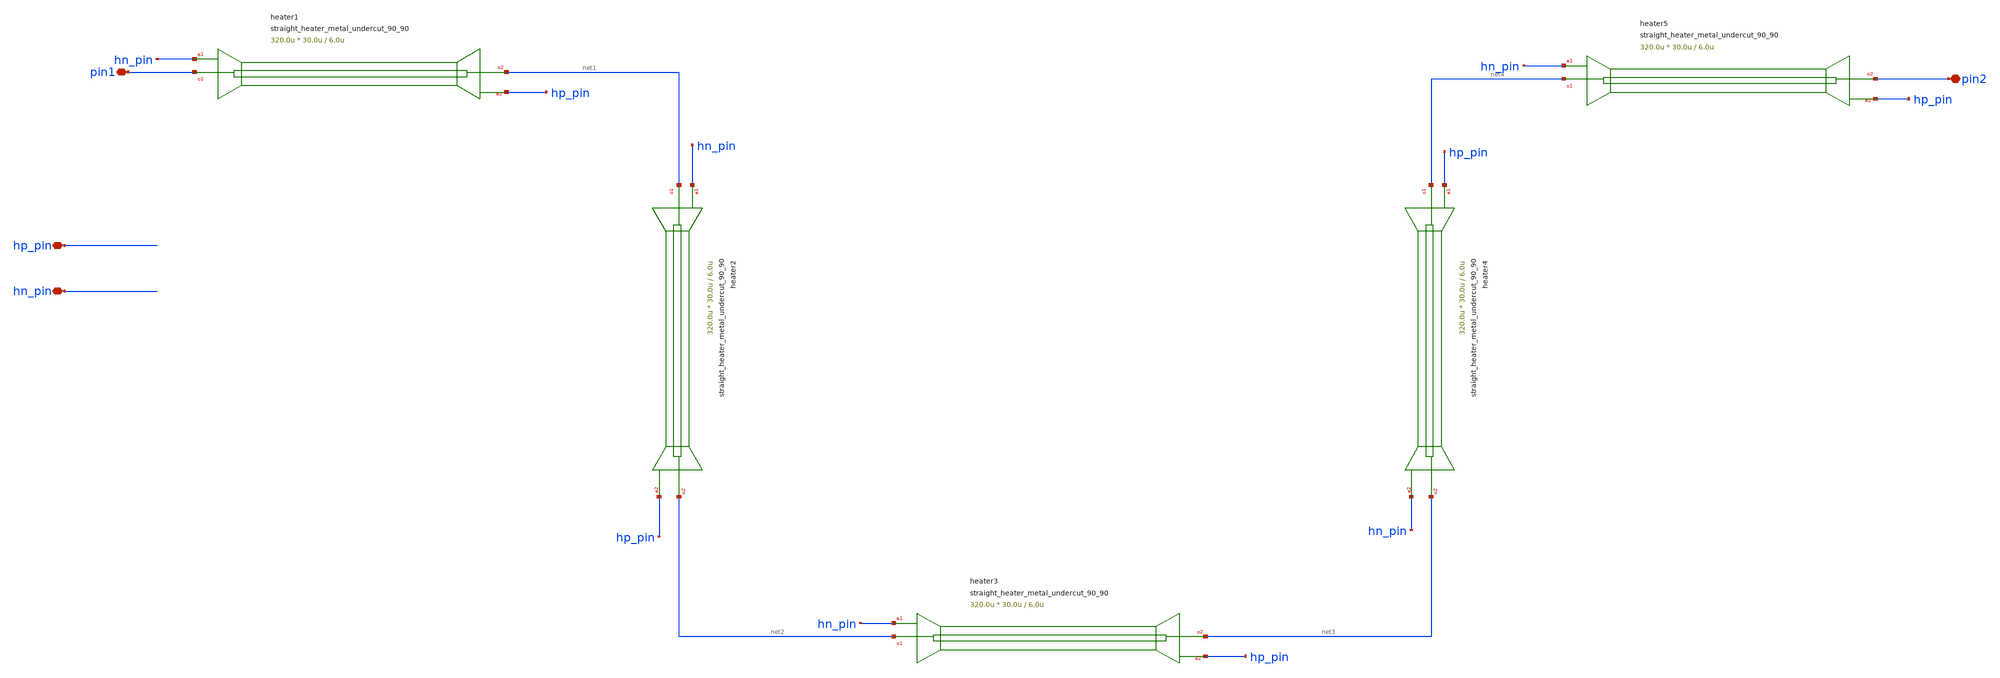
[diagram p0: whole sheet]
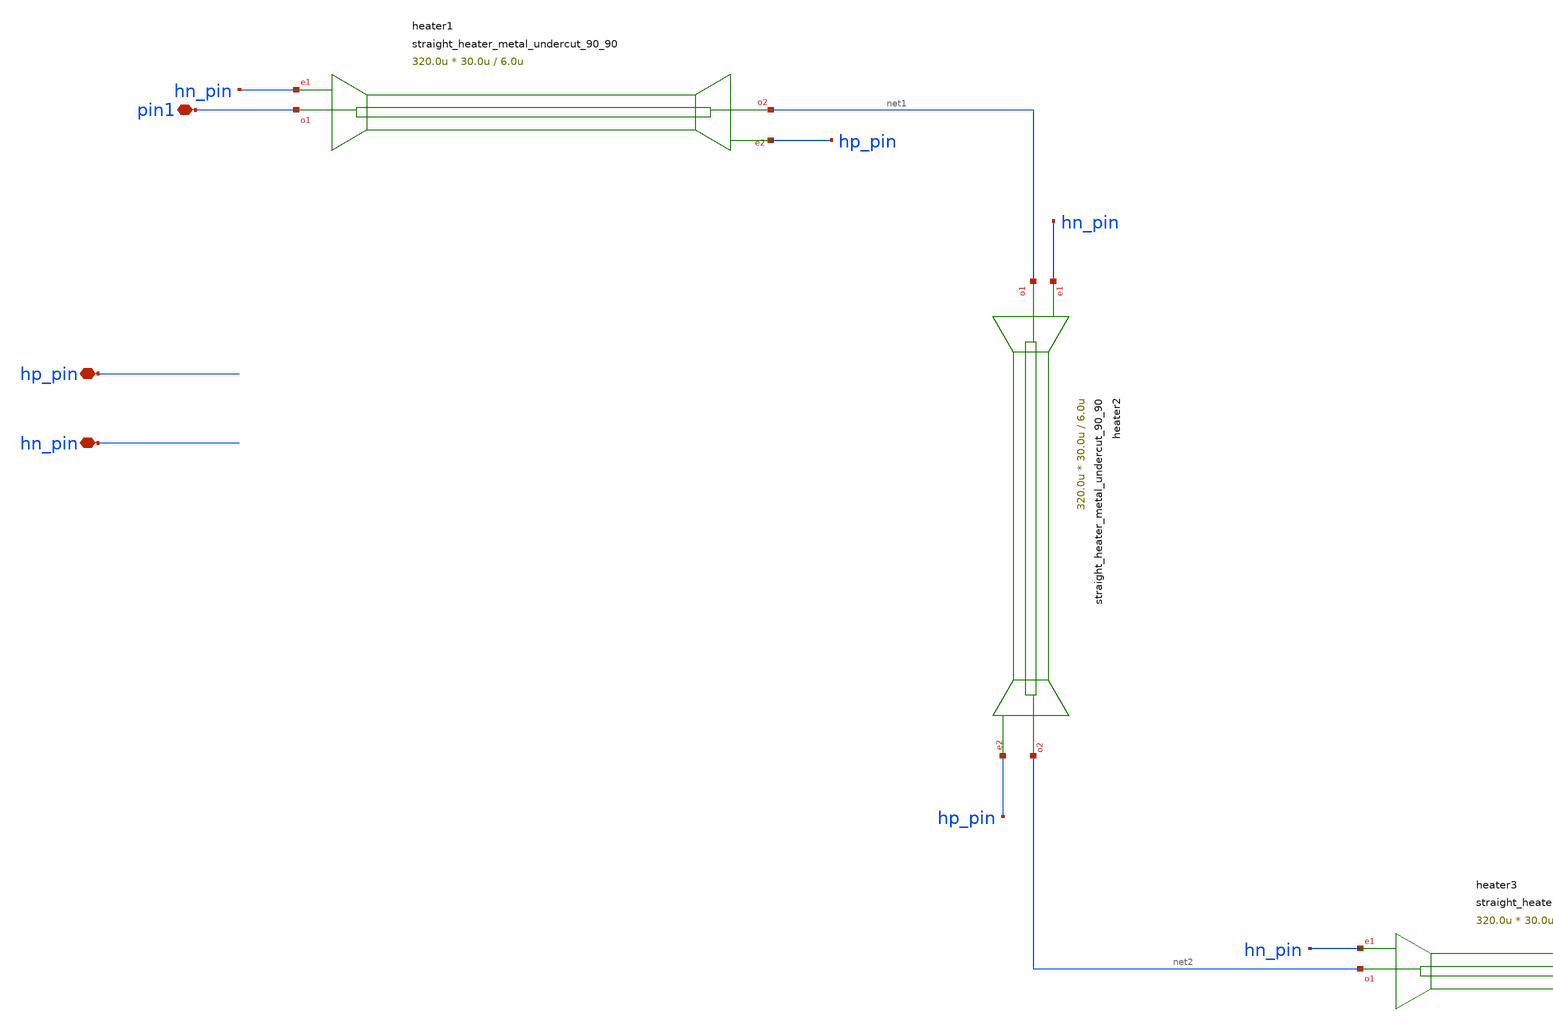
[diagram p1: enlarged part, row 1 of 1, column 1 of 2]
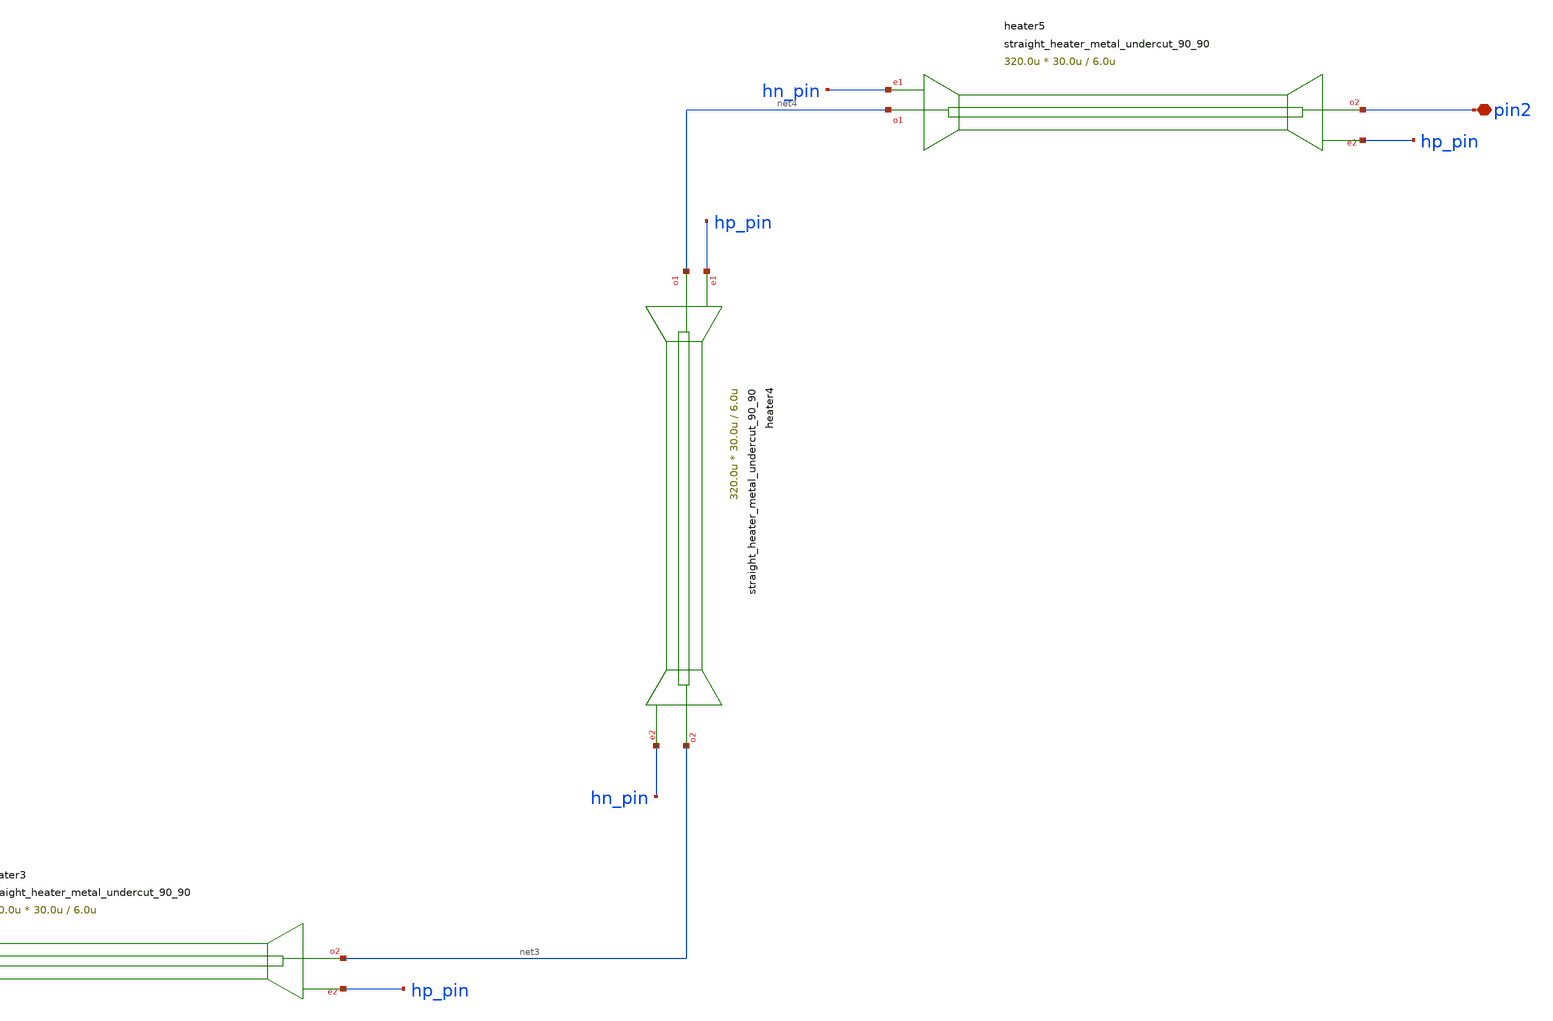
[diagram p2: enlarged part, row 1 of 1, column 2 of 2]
** sch_path: xschem/tests/test_sch/test_straight_heater_metal_undercut_90_90.sch
* Copyright (c) 2024, Mabrains LLC
* Licensed under the GNU Lesser General Public License, Version 3.0 (the "License");
* you may not use this file except in compliance with the License.
* GNU Lesser General Public License
* Version 3, 29 June 2007
* This program is free software: you can redistribute it and/or modify
* it under the terms of the GNU Lesser General Public License as published
* by the Free Software Foundation, either version 3 of the License, or
* (at your option) any later version.
* This program is distributed in the hope that it will be useful,
* but WITHOUT ANY WARRANTY; without even the implied warranty of
* MERCHANTABILITY or FITNESS FOR A PARTICULAR PURPOSE.  See the
* GNU Lesser General Public License for more details.
* You should have received a copy of the GNU Lesser General Public License
* along with this program.  If not, see <https://www.gnu.org/licenses/>.
* SPDX-License-Identifier: LGPL-3.0
**.subckt test_straight_heater_metal_undercut_90_90 hp_pin hn_pin pin1 pin2
*.iopin hp_pin
*.iopin hn_pin
*.iopin pin1
*.iopin pin2
Pheater1 pin1 net1 hn_pin hp_pin straight_heater_metal_undercut_90_90 length=320.0u
+ length_undercut_spacing=6.0u length_undercut=30.0u length_straight_input=15.0u heater_taper_length=5.0u
Pheater2 net1 net2 hn_pin hp_pin straight_heater_metal_undercut_90_90 length=320.0u
+ length_undercut_spacing=6.0u length_undercut=30.0u length_straight_input=15.0u heater_taper_length=5.0u
Pheater3 net2 net3 hn_pin hp_pin straight_heater_metal_undercut_90_90 length=320.0u
+ length_undercut_spacing=6.0u length_undercut=30.0u length_straight_input=15.0u heater_taper_length=5.0u
Pheater4 net4 net3 hp_pin hn_pin straight_heater_metal_undercut_90_90 length=320.0u
+ length_undercut_spacing=6.0u length_undercut=30.0u length_straight_input=15.0u heater_taper_length=5.0u
Pheater5 net4 pin2 hn_pin hp_pin straight_heater_metal_undercut_90_90 length=320.0u
+ length_undercut_spacing=6.0u length_undercut=30.0u length_straight_input=15.0u heater_taper_length=5.0u
**.ends
.end
